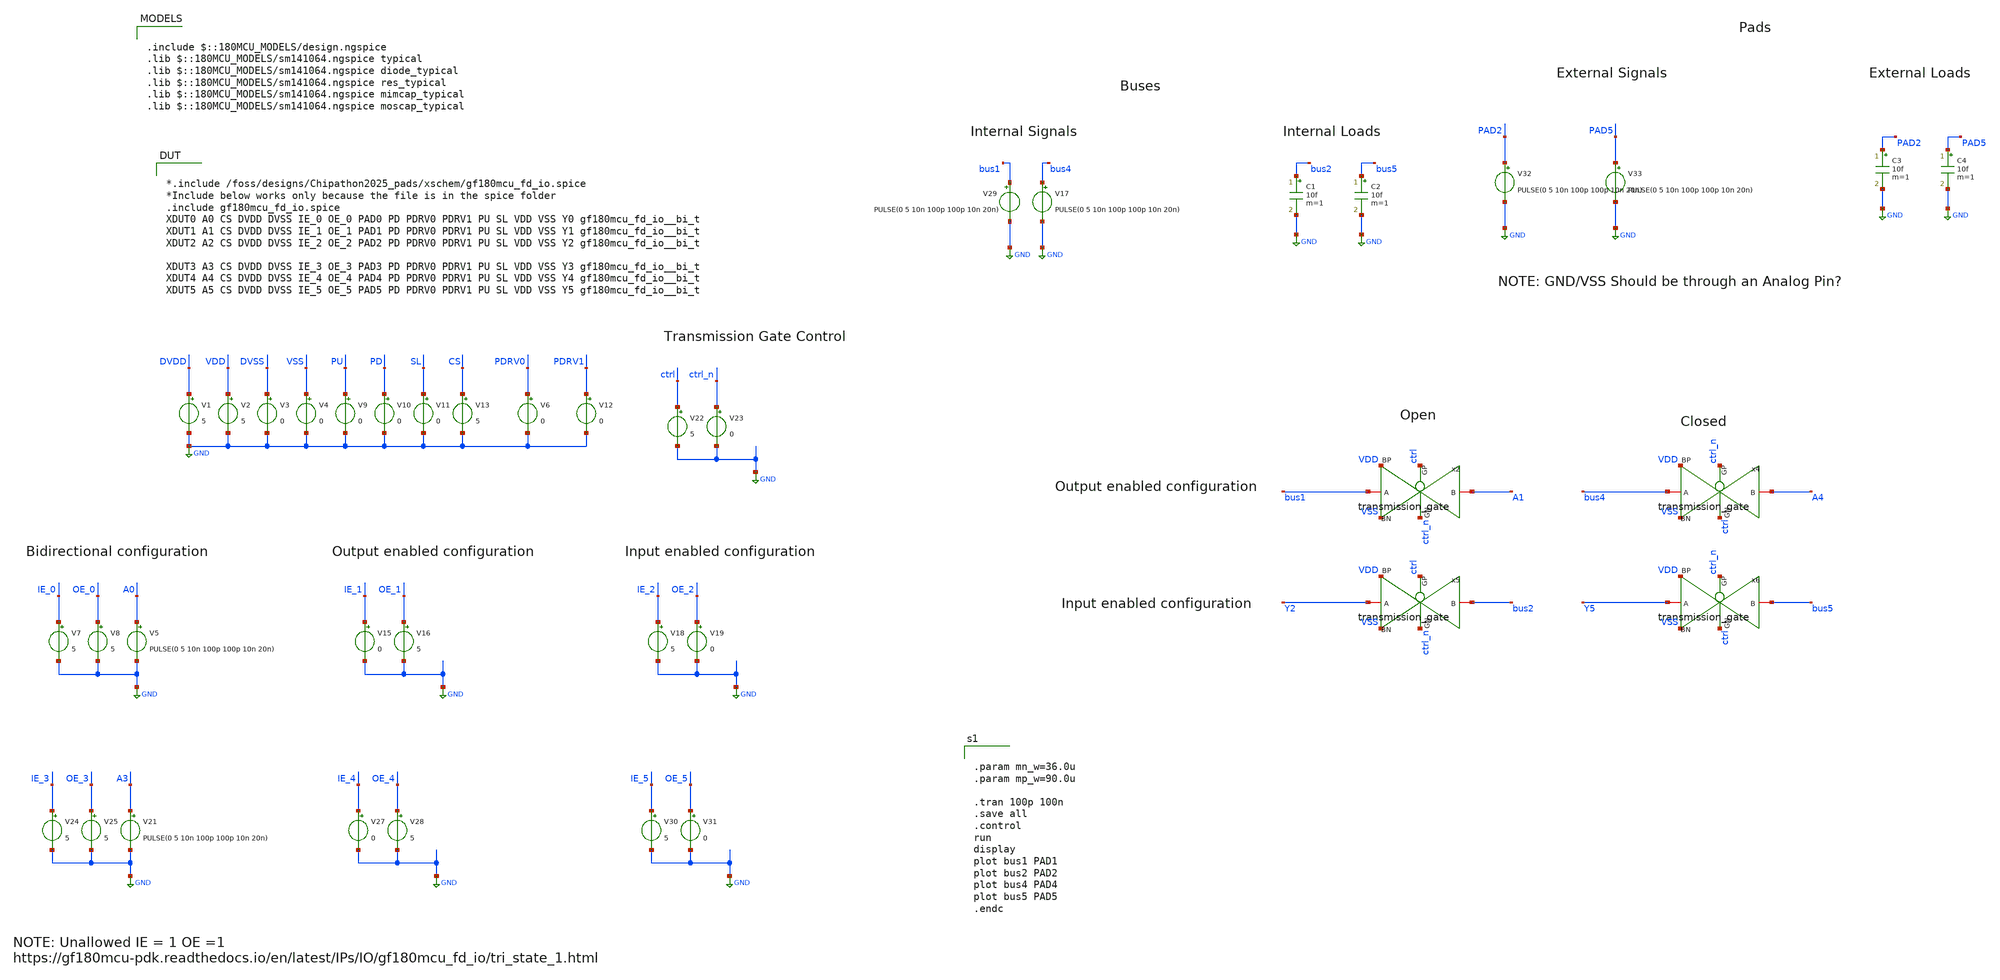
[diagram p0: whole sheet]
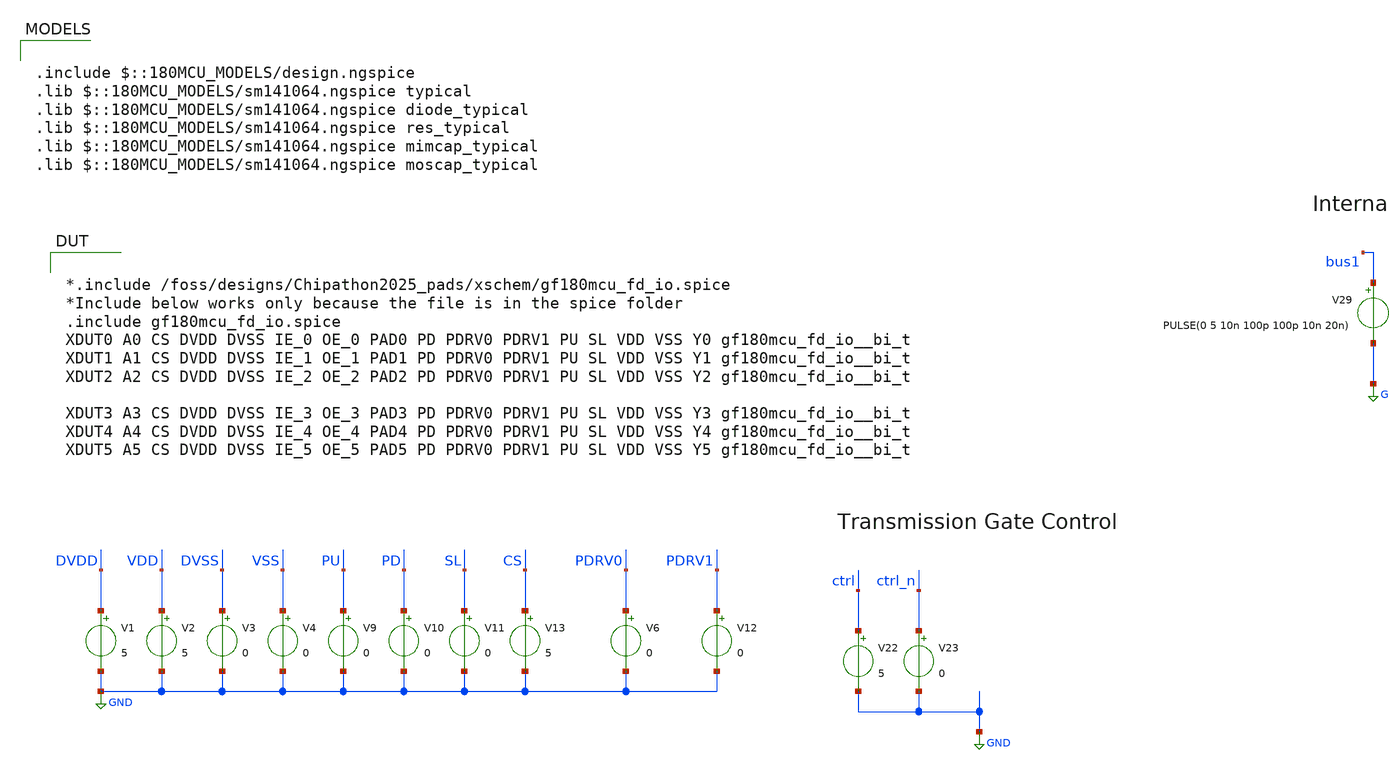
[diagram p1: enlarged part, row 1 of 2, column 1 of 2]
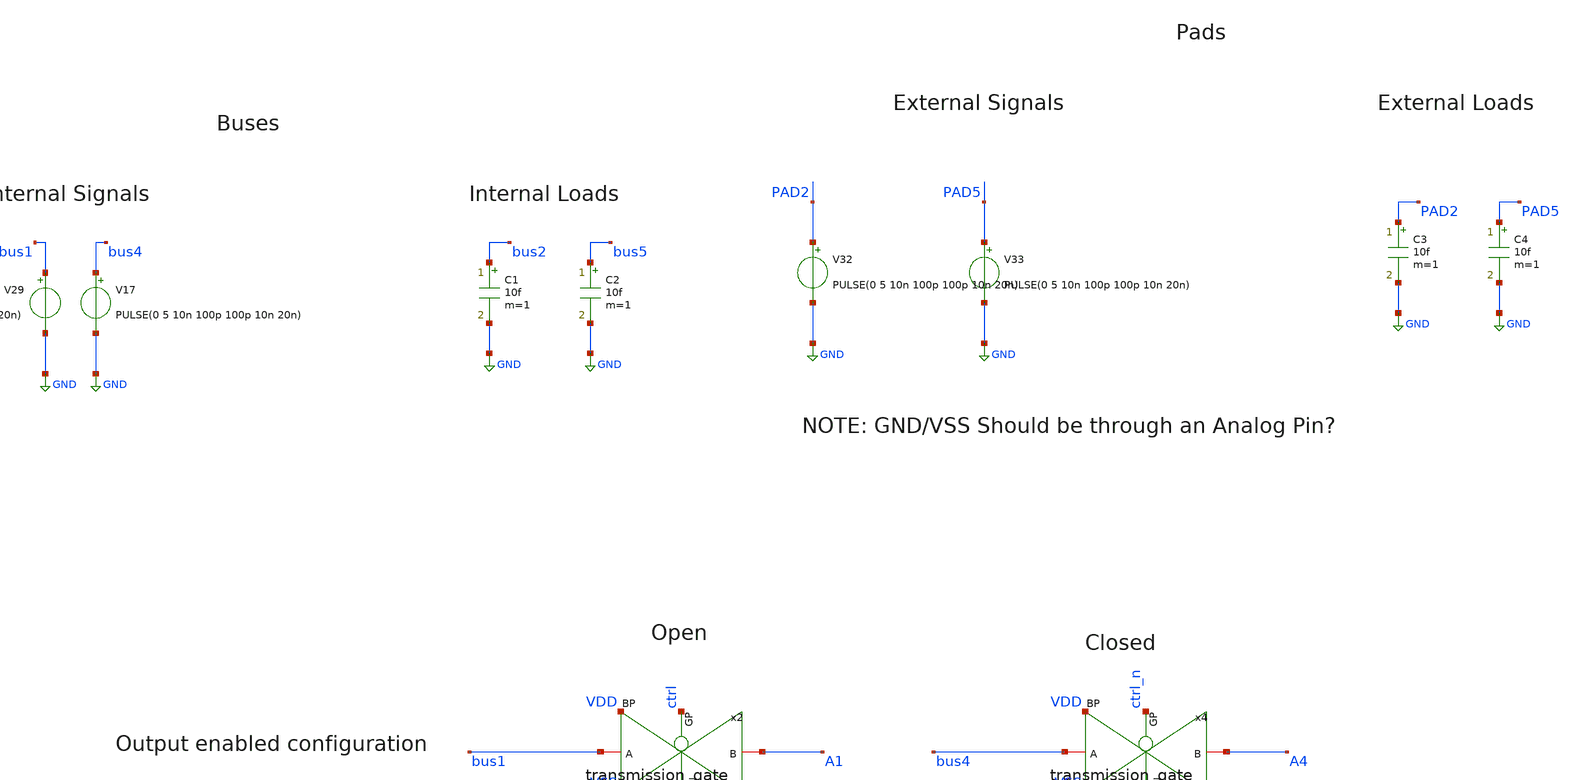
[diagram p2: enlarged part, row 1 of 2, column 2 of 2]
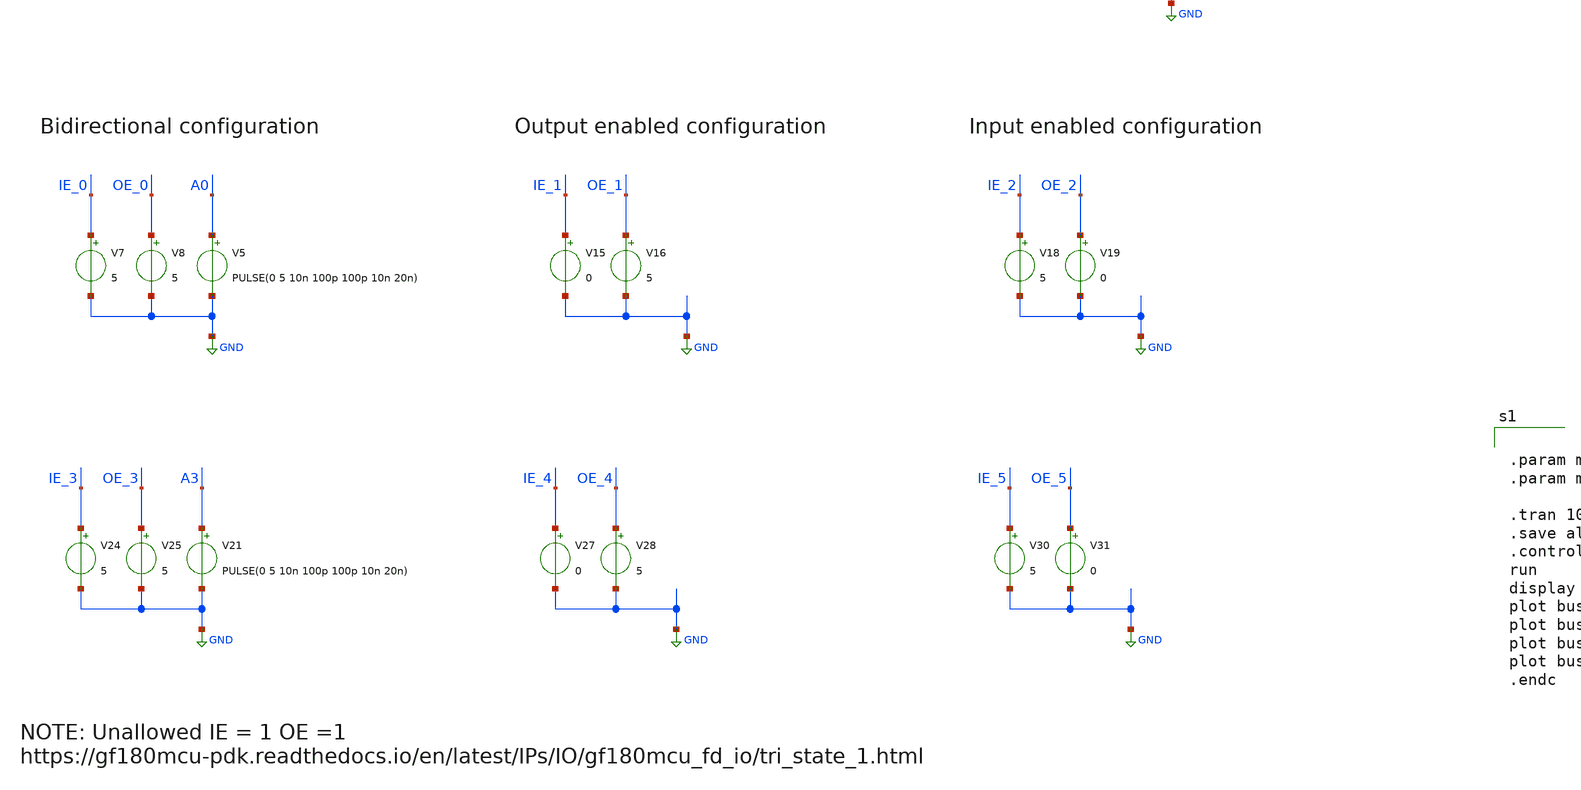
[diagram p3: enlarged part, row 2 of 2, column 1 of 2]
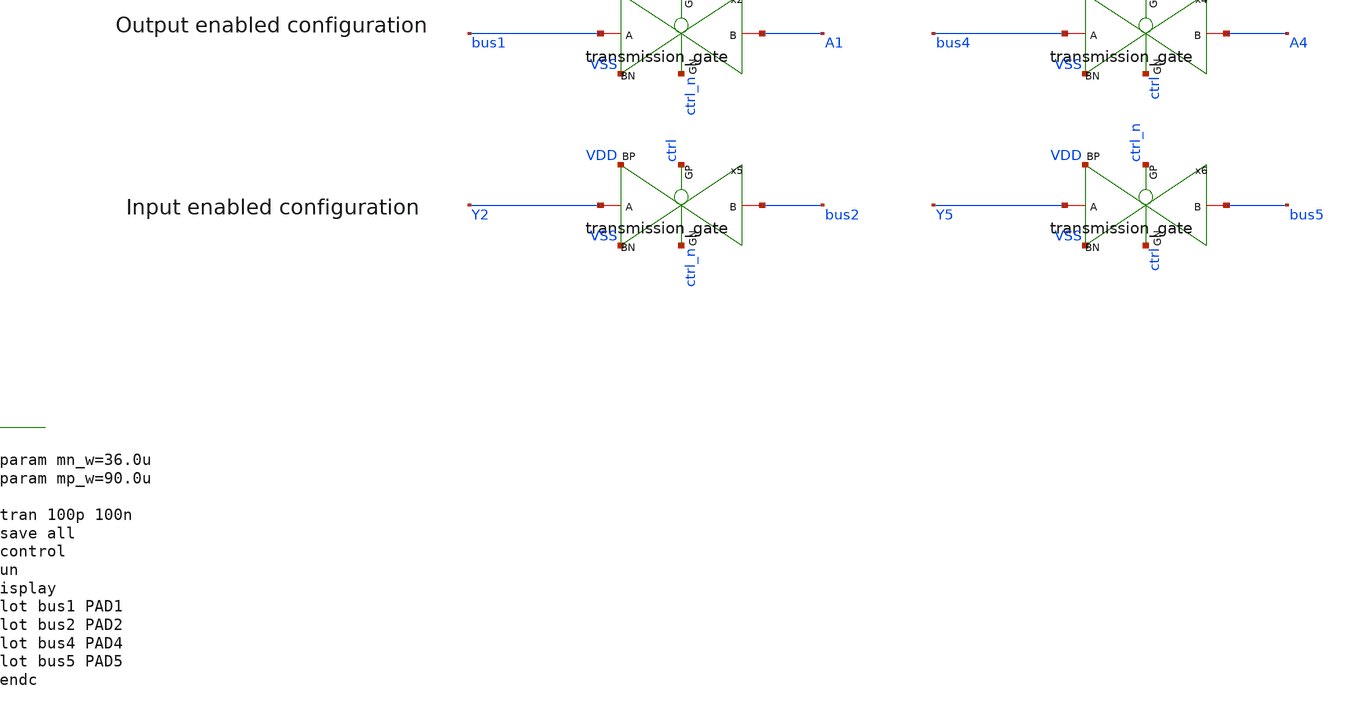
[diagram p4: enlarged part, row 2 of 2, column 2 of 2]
** sch_path: xschem/gf180mcu_io/bi_t_tran_tb.sch
**.subckt bi_t_tran_tb
V1 DVDD GND 5
V2 VDD GND 5
V3 DVSS GND 0
V4 VSS GND 0
V5 A0 GND PULSE(0 5 10n 100p 100p 10n 20n)
V7 IE_0 GND 5
V8 OE_0 GND 5
V9 PU GND 0
V10 PD GND 0
V11 SL GND 0
V13 CS GND 5
V6 PDRV0 GND 0
V12 PDRV1 GND 0
V15 IE_1 GND 0
V16 OE_1 GND 5
V18 IE_2 GND 5
V19 OE_2 GND 0
x2 A1 ctrl_n ctrl bus1 VDD VSS transmission_gate
V22 ctrl GND 5
V23 ctrl_n GND 0
x4 A4 ctrl ctrl_n bus4 VDD VSS transmission_gate
x5 bus2 ctrl_n ctrl Y2 VDD VSS transmission_gate
x6 bus5 ctrl ctrl_n Y5 VDD VSS transmission_gate
V21 A3 GND PULSE(0 5 10n 100p 100p 10n 20n)
V24 IE_3 GND 5
V25 OE_3 GND 5
V27 IE_4 GND 0
V28 OE_4 GND 5
V30 IE_5 GND 5
V31 OE_5 GND 0
V32 PAD2 GND PULSE(0 5 10n 100p 100p 10n 20n)
V33 PAD5 GND PULSE(0 5 10n 100p 100p 10n 20n)
V17 bus4 GND PULSE(0 5 10n 100p 100p 10n 20n)
V29 bus1 GND PULSE(0 5 10n 100p 100p 10n 20n)
C1 bus2 GND 10f m=1
C2 bus5 GND 10f m=1
C3 PAD2 GND 10f m=1
C4 PAD5 GND 10f m=1
**** begin user architecture code


.param mn_w=36.0u
.param mp_w=90.0u

.tran 100p 100n
.save all
.control
run
display
plot bus1 PAD1
plot bus2 PAD2
plot bus4 PAD4
plot bus5 PAD5
.endc



.include $::180MCU_MODELS/design.ngspice
.lib $::180MCU_MODELS/sm141064.ngspice typical
.lib $::180MCU_MODELS/sm141064.ngspice diode_typical
.lib $::180MCU_MODELS/sm141064.ngspice res_typical
.lib $::180MCU_MODELS/sm141064.ngspice mimcap_typical
.lib $::180MCU_MODELS/sm141064.ngspice moscap_typical


*.include /foss/designs/Chipathon2025_pads/xschem/gf180mcu_fd_io.spice
*Include below works only because the file is in the spice folder
.include gf180mcu_fd_io.spice
XDUT0 A0 CS DVDD DVSS IE_0 OE_0 PAD0 PD PDRV0 PDRV1 PU SL VDD VSS Y0 gf180mcu_fd_io__bi_t
XDUT1 A1 CS DVDD DVSS IE_1 OE_1 PAD1 PD PDRV0 PDRV1 PU SL VDD VSS Y1 gf180mcu_fd_io__bi_t
XDUT2 A2 CS DVDD DVSS IE_2 OE_2 PAD2 PD PDRV0 PDRV1 PU SL VDD VSS Y2 gf180mcu_fd_io__bi_t

XDUT3 A3 CS DVDD DVSS IE_3 OE_3 PAD3 PD PDRV0 PDRV1 PU SL VDD VSS Y3 gf180mcu_fd_io__bi_t
XDUT4 A4 CS DVDD DVSS IE_4 OE_4 PAD4 PD PDRV0 PDRV1 PU SL VDD VSS Y4 gf180mcu_fd_io__bi_t
XDUT5 A5 CS DVDD DVSS IE_5 OE_5 PAD5 PD PDRV0 PDRV1 PU SL VDD VSS Y5 gf180mcu_fd_io__bi_t


**** end user architecture code
**.ends

* expanding   symbol:  tgate/transmission_gate.sym # of pins=6
** sym_path: tgate/transmission_gate.sym
** sch_path: tgate/transmission_gate.sch
.subckt transmission_gate B GN GP A BP BN
*.iopin B
*.iopin GN
*.iopin A
*.iopin GP
*.iopin BN
*.iopin BP
XM1 A GN B BN nfet_03v3 L=0.28u W=36u nf=6 ad='int((nf+1)/2) * W/nf * 0.18u' as='int((nf+2)/2) * W/nf * 0.18u'
+ pd='2*int((nf+1)/2) * (W/nf + 0.18u)' ps='2*int((nf+2)/2) * (W/nf + 0.18u)' nrd='0.18u / W' nrs='0.18u / W'
+ sa=0 sb=0 sd=0 m=1
XM2 A GP B BP pfet_03v3 L=0.28u W=90u nf=6 ad='int((nf+1)/2) * W/nf * 0.18u' as='int((nf+2)/2) * W/nf * 0.18u'
+ pd='2*int((nf+1)/2) * (W/nf + 0.18u)' ps='2*int((nf+2)/2) * (W/nf + 0.18u)' nrd='0.18u / W' nrs='0.18u / W'
+ sa=0 sb=0 sd=0 m=1
.ends

.GLOBAL GND
.end
